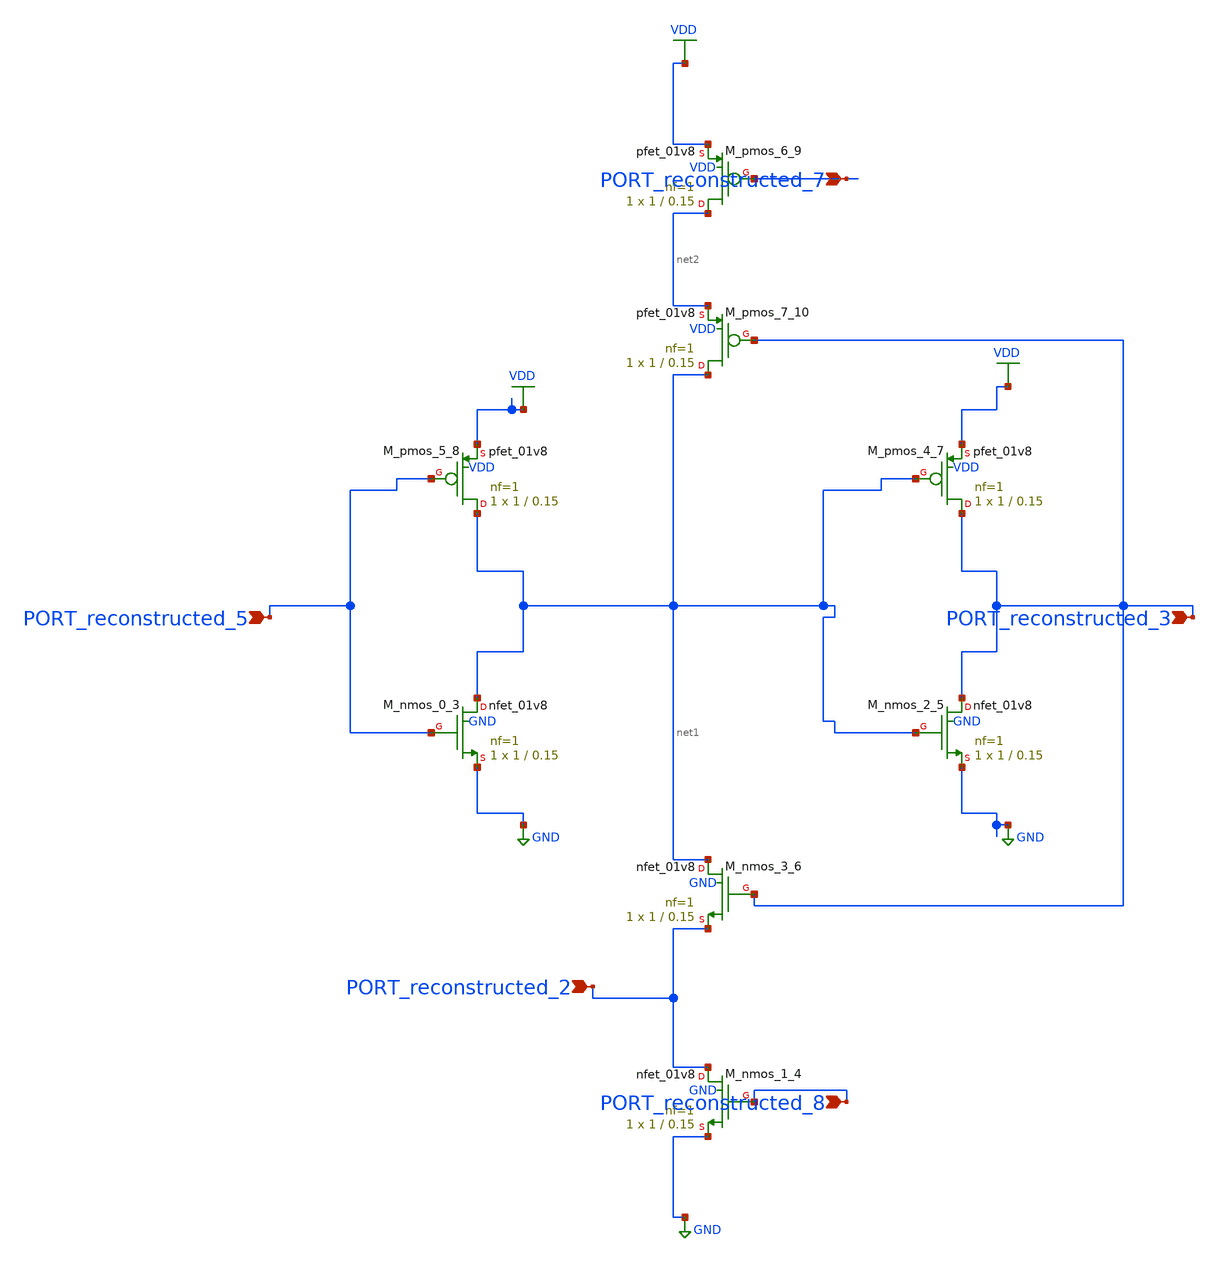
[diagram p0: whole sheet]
** sch_path: schematics/10_1109_ACCESS_2023_3241492_03_001_crop1.sch
**.subckt 10_1109_ACCESS_2023_3241492_03_001_crop1 PORT_reconstructed_2 PORT_reconstructed_3
*+ PORT_reconstructed_7 PORT_reconstructed_5 PORT_reconstructed_8
*.ipin PORT_reconstructed_2
*.ipin PORT_reconstructed_3
*.ipin PORT_reconstructed_7
*.ipin PORT_reconstructed_5
*.ipin PORT_reconstructed_8
XM_nmos_0_3 net1 PORT_reconstructed_5 GND GND sky130_fd_pr__nfet_01v8 L=0.15 W=1 nf=1 ad='int((1 + 1)/2) * 1 / 1 * 0.29'
+ as='int((1 + 2)/2) * 1 / 1 * 0.29' pd='2*int((1 + 1)/2) * (1 / 1 + 0.29)' ps='2*int((1 + 2)/2) * (1 / 1 + 0.29)'
+ nrd='0.29 / 1 ' nrs='0.29 / 1 ' sa=0 sb=0 sd=0 mult=1 m=1
XM_nmos_1_4 PORT_reconstructed_2 PORT_reconstructed_8 GND GND sky130_fd_pr__nfet_01v8 L=0.15 W=1 nf=1
+ ad='int((1 + 1)/2) * 1 / 1 * 0.29' as='int((1 + 2)/2) * 1 / 1 * 0.29' pd='2*int((1 + 1)/2) * (1 / 1 + 0.29)'
+ ps='2*int((1 + 2)/2) * (1 / 1 + 0.29)' nrd='0.29 / 1 ' nrs='0.29 / 1 ' sa=0 sb=0 sd=0 mult=1 m=1
XM_nmos_2_5 PORT_reconstructed_3 net1 GND GND sky130_fd_pr__nfet_01v8 L=0.15 W=1 nf=1 ad='int((1 + 1)/2) * 1 / 1 * 0.29'
+ as='int((1 + 2)/2) * 1 / 1 * 0.29' pd='2*int((1 + 1)/2) * (1 / 1 + 0.29)' ps='2*int((1 + 2)/2) * (1 / 1 + 0.29)'
+ nrd='0.29 / 1 ' nrs='0.29 / 1 ' sa=0 sb=0 sd=0 mult=1 m=1
XM_nmos_3_6 net1 PORT_reconstructed_3 PORT_reconstructed_2 GND sky130_fd_pr__nfet_01v8 L=0.15 W=1 nf=1
+ ad='int((1 + 1)/2) * 1 / 1 * 0.29' as='int((1 + 2)/2) * 1 / 1 * 0.29' pd='2*int((1 + 1)/2) * (1 / 1 + 0.29)'
+ ps='2*int((1 + 2)/2) * (1 / 1 + 0.29)' nrd='0.29 / 1 ' nrs='0.29 / 1 ' sa=0 sb=0 sd=0 mult=1 m=1
XM_pmos_4_7 PORT_reconstructed_3 net1 VDD VDD sky130_fd_pr__pfet_01v8 L=0.15 W=1 nf=1 ad='int((1 + 1)/2) * 1 / 1 * 0.29'
+ as='int((1 + 2)/2) * 1 / 1 * 0.29' pd='2*int((1 + 1)/2) * (1 / 1 + 0.29)' ps='2*int((1 + 2)/2) * (1 / 1 + 0.29)'
+ nrd='0.29 / 1 ' nrs='0.29 / 1 ' sa=0 sb=0 sd=0 mult=1 m=1
XM_pmos_5_8 net1 PORT_reconstructed_5 VDD VDD sky130_fd_pr__pfet_01v8 L=0.15 W=1 nf=1 ad='int((1 + 1)/2) * 1 / 1 * 0.29'
+ as='int((1 + 2)/2) * 1 / 1 * 0.29' pd='2*int((1 + 1)/2) * (1 / 1 + 0.29)' ps='2*int((1 + 2)/2) * (1 / 1 + 0.29)'
+ nrd='0.29 / 1 ' nrs='0.29 / 1 ' sa=0 sb=0 sd=0 mult=1 m=1
XM_pmos_6_9 net2 PORT_reconstructed_7 VDD VDD sky130_fd_pr__pfet_01v8 L=0.15 W=1 nf=1 ad='int((1 + 1)/2) * 1 / 1 * 0.29'
+ as='int((1 + 2)/2) * 1 / 1 * 0.29' pd='2*int((1 + 1)/2) * (1 / 1 + 0.29)' ps='2*int((1 + 2)/2) * (1 / 1 + 0.29)'
+ nrd='0.29 / 1 ' nrs='0.29 / 1 ' sa=0 sb=0 sd=0 mult=1 m=1
XM_pmos_7_10 net1 PORT_reconstructed_3 net2 VDD sky130_fd_pr__pfet_01v8 L=0.15 W=1 nf=1 ad='int((1 + 1)/2) * 1 / 1 * 0.29'
+ as='int((1 + 2)/2) * 1 / 1 * 0.29' pd='2*int((1 + 1)/2) * (1 / 1 + 0.29)' ps='2*int((1 + 2)/2) * (1 / 1 + 0.29)'
+ nrd='0.29 / 1 ' nrs='0.29 / 1 ' sa=0 sb=0 sd=0 mult=1 m=1
**.ends
.GLOBAL GND
.GLOBAL VDD
.end
